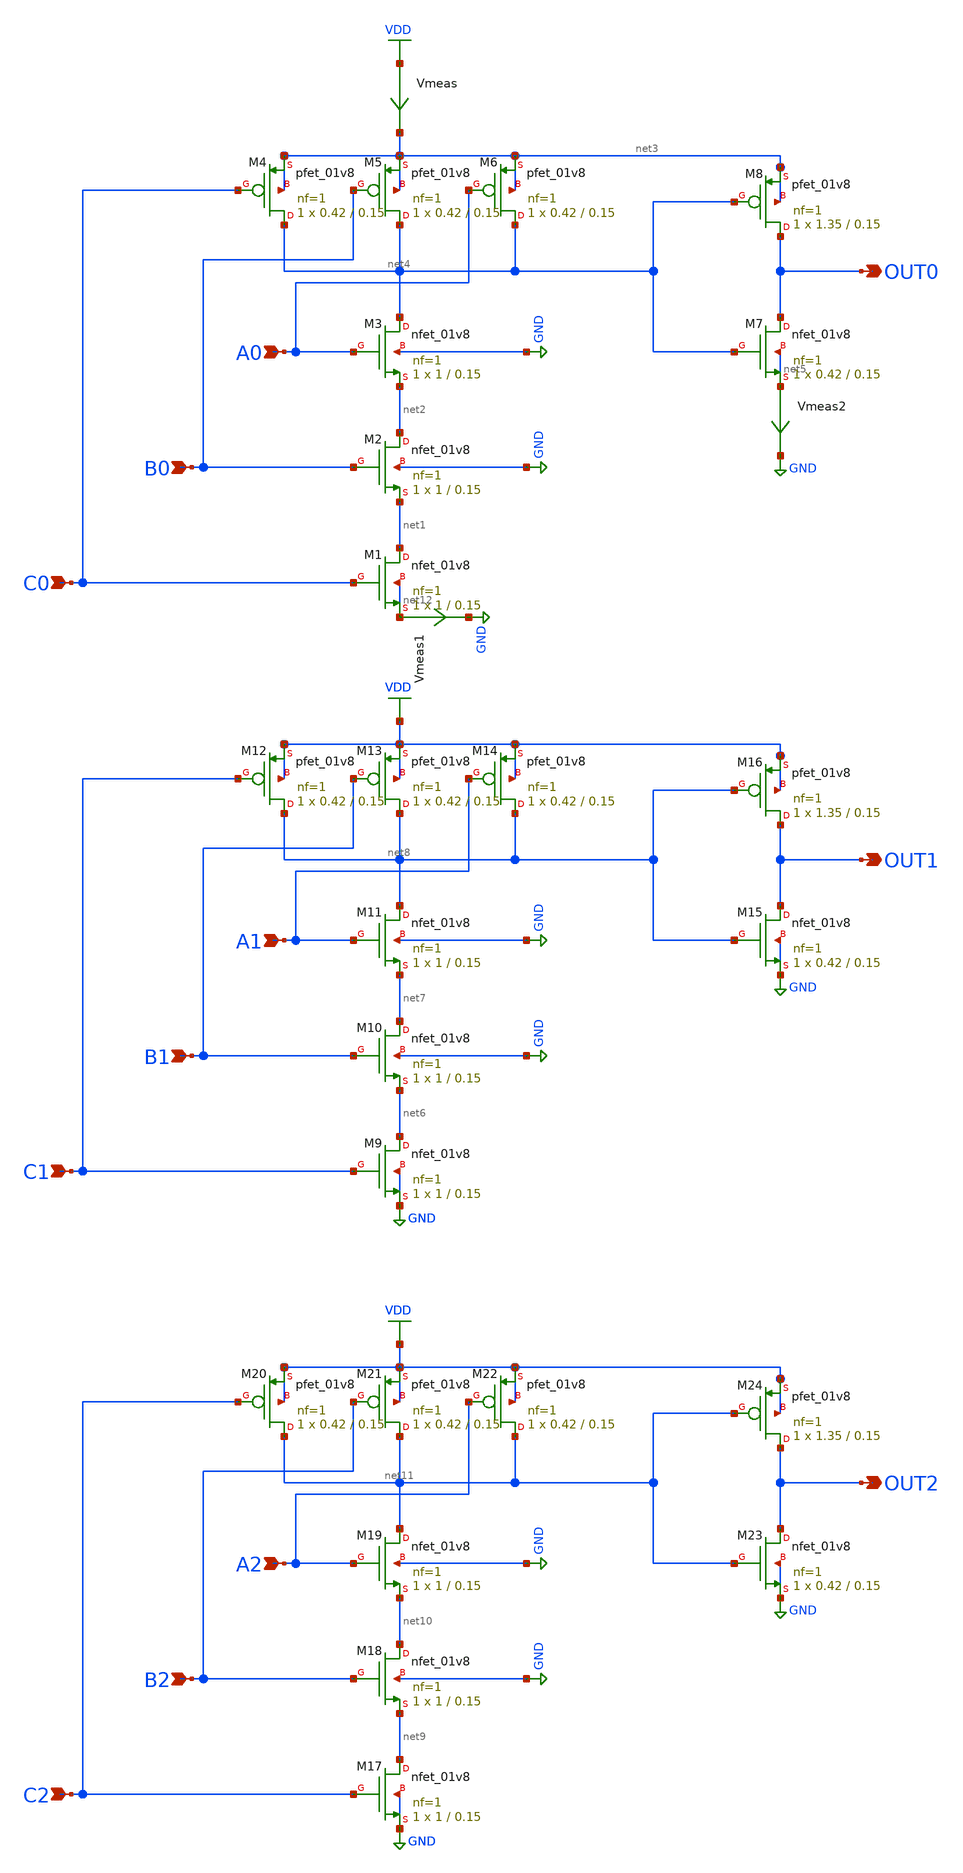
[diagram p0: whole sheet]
** sch_path: xschem/dec_cell_3.sch
**.subckt dec_cell_3 OUT0 OUT1 OUT2 C2 B2 A2 C1 B1 A1 C0 B0 A0
*.opin OUT0
*.opin OUT1
*.opin OUT2
*.ipin C2
*.ipin B2
*.ipin A2
*.ipin C1
*.ipin B1
*.ipin A1
*.ipin C0
*.ipin B0
*.ipin A0
XM1 net1 C0 net12 net12 sky130_fd_pr__nfet_01v8 L=0.15 W=1 nf=1 ad='int((nf+1)/2) * W/nf * 0.29' as='int((nf+2)/2) * W/nf * 0.29'
+ pd='2*int((nf+1)/2) * (W/nf + 0.29)' ps='2*int((nf+2)/2) * (W/nf + 0.29)' nrd='0.29 / W' nrs='0.29 / W'
+ sa=0 sb=0 sd=0 mult=1 m=1
XM2 net2 B0 net1 GND sky130_fd_pr__nfet_01v8 L=0.15 W=1 nf=1 ad='int((nf+1)/2) * W/nf * 0.29' as='int((nf+2)/2) * W/nf * 0.29'
+ pd='2*int((nf+1)/2) * (W/nf + 0.29)' ps='2*int((nf+2)/2) * (W/nf + 0.29)' nrd='0.29 / W' nrs='0.29 / W'
+ sa=0 sb=0 sd=0 mult=1 m=1
XM3 net4 A0 net2 GND sky130_fd_pr__nfet_01v8 L=0.15 W=1 nf=1 ad='int((nf+1)/2) * W/nf * 0.29' as='int((nf+2)/2) * W/nf * 0.29'
+ pd='2*int((nf+1)/2) * (W/nf + 0.29)' ps='2*int((nf+2)/2) * (W/nf + 0.29)' nrd='0.29 / W' nrs='0.29 / W'
+ sa=0 sb=0 sd=0 mult=1 m=1
XM4 net4 C0 net3 net3 sky130_fd_pr__pfet_01v8 L=0.15 W=0.42 nf=1 ad='int((nf+1)/2) * W/nf * 0.29' as='int((nf+2)/2) * W/nf * 0.29'
+ pd='2*int((nf+1)/2) * (W/nf + 0.29)' ps='2*int((nf+2)/2) * (W/nf + 0.29)' nrd='0.29 / W' nrs='0.29 / W'
+ sa=0 sb=0 sd=0 mult=1 m=1
XM5 net4 B0 net3 net3 sky130_fd_pr__pfet_01v8 L=0.15 W=0.42 nf=1 ad='int((nf+1)/2) * W/nf * 0.29' as='int((nf+2)/2) * W/nf * 0.29'
+ pd='2*int((nf+1)/2) * (W/nf + 0.29)' ps='2*int((nf+2)/2) * (W/nf + 0.29)' nrd='0.29 / W' nrs='0.29 / W'
+ sa=0 sb=0 sd=0 mult=1 m=1
XM6 net4 A0 net3 net3 sky130_fd_pr__pfet_01v8 L=0.15 W=0.42 nf=1 ad='int((nf+1)/2) * W/nf * 0.29' as='int((nf+2)/2) * W/nf * 0.29'
+ pd='2*int((nf+1)/2) * (W/nf + 0.29)' ps='2*int((nf+2)/2) * (W/nf + 0.29)' nrd='0.29 / W' nrs='0.29 / W'
+ sa=0 sb=0 sd=0 mult=1 m=1
XM7 OUT0 net4 net5 net5 sky130_fd_pr__nfet_01v8 L=0.15 W=0.42 nf=1 ad='int((nf+1)/2) * W/nf * 0.29' as='int((nf+2)/2) * W/nf * 0.29'
+ pd='2*int((nf+1)/2) * (W/nf + 0.29)' ps='2*int((nf+2)/2) * (W/nf + 0.29)' nrd='0.29 / W' nrs='0.29 / W'
+ sa=0 sb=0 sd=0 mult=1 m=1
XM8 OUT0 net4 net3 net3 sky130_fd_pr__pfet_01v8 L=0.15 W=1.35 nf=1 ad='int((nf+1)/2) * W/nf * 0.29' as='int((nf+2)/2) * W/nf * 0.29'
+ pd='2*int((nf+1)/2) * (W/nf + 0.29)' ps='2*int((nf+2)/2) * (W/nf + 0.29)' nrd='0.29 / W' nrs='0.29 / W'
+ sa=0 sb=0 sd=0 mult=1 m=1
XM9 net6 C1 GND GND sky130_fd_pr__nfet_01v8 L=0.15 W=1 nf=1 ad='int((nf+1)/2) * W/nf * 0.29' as='int((nf+2)/2) * W/nf * 0.29'
+ pd='2*int((nf+1)/2) * (W/nf + 0.29)' ps='2*int((nf+2)/2) * (W/nf + 0.29)' nrd='0.29 / W' nrs='0.29 / W'
+ sa=0 sb=0 sd=0 mult=1 m=1
XM10 net7 B1 net6 GND sky130_fd_pr__nfet_01v8 L=0.15 W=1 nf=1 ad='int((nf+1)/2) * W/nf * 0.29' as='int((nf+2)/2) * W/nf * 0.29'
+ pd='2*int((nf+1)/2) * (W/nf + 0.29)' ps='2*int((nf+2)/2) * (W/nf + 0.29)' nrd='0.29 / W' nrs='0.29 / W'
+ sa=0 sb=0 sd=0 mult=1 m=1
XM11 net8 A1 net7 GND sky130_fd_pr__nfet_01v8 L=0.15 W=1 nf=1 ad='int((nf+1)/2) * W/nf * 0.29' as='int((nf+2)/2) * W/nf * 0.29'
+ pd='2*int((nf+1)/2) * (W/nf + 0.29)' ps='2*int((nf+2)/2) * (W/nf + 0.29)' nrd='0.29 / W' nrs='0.29 / W'
+ sa=0 sb=0 sd=0 mult=1 m=1
XM12 net8 C1 VDD VDD sky130_fd_pr__pfet_01v8 L=0.15 W=0.42 nf=1 ad='int((nf+1)/2) * W/nf * 0.29' as='int((nf+2)/2) * W/nf * 0.29'
+ pd='2*int((nf+1)/2) * (W/nf + 0.29)' ps='2*int((nf+2)/2) * (W/nf + 0.29)' nrd='0.29 / W' nrs='0.29 / W'
+ sa=0 sb=0 sd=0 mult=1 m=1
XM13 net8 B1 VDD VDD sky130_fd_pr__pfet_01v8 L=0.15 W=0.42 nf=1 ad='int((nf+1)/2) * W/nf * 0.29' as='int((nf+2)/2) * W/nf * 0.29'
+ pd='2*int((nf+1)/2) * (W/nf + 0.29)' ps='2*int((nf+2)/2) * (W/nf + 0.29)' nrd='0.29 / W' nrs='0.29 / W'
+ sa=0 sb=0 sd=0 mult=1 m=1
XM14 net8 A1 VDD VDD sky130_fd_pr__pfet_01v8 L=0.15 W=0.42 nf=1 ad='int((nf+1)/2) * W/nf * 0.29' as='int((nf+2)/2) * W/nf * 0.29'
+ pd='2*int((nf+1)/2) * (W/nf + 0.29)' ps='2*int((nf+2)/2) * (W/nf + 0.29)' nrd='0.29 / W' nrs='0.29 / W'
+ sa=0 sb=0 sd=0 mult=1 m=1
XM15 OUT1 net8 GND GND sky130_fd_pr__nfet_01v8 L=0.15 W=0.42 nf=1 ad='int((nf+1)/2) * W/nf * 0.29' as='int((nf+2)/2) * W/nf * 0.29'
+ pd='2*int((nf+1)/2) * (W/nf + 0.29)' ps='2*int((nf+2)/2) * (W/nf + 0.29)' nrd='0.29 / W' nrs='0.29 / W'
+ sa=0 sb=0 sd=0 mult=1 m=1
XM16 OUT1 net8 VDD VDD sky130_fd_pr__pfet_01v8 L=0.15 W=1.35 nf=1 ad='int((nf+1)/2) * W/nf * 0.29' as='int((nf+2)/2) * W/nf * 0.29'
+ pd='2*int((nf+1)/2) * (W/nf + 0.29)' ps='2*int((nf+2)/2) * (W/nf + 0.29)' nrd='0.29 / W' nrs='0.29 / W'
+ sa=0 sb=0 sd=0 mult=1 m=1
XM17 net9 C2 GND GND sky130_fd_pr__nfet_01v8 L=0.15 W=1 nf=1 ad='int((nf+1)/2) * W/nf * 0.29' as='int((nf+2)/2) * W/nf * 0.29'
+ pd='2*int((nf+1)/2) * (W/nf + 0.29)' ps='2*int((nf+2)/2) * (W/nf + 0.29)' nrd='0.29 / W' nrs='0.29 / W'
+ sa=0 sb=0 sd=0 mult=1 m=1
XM18 net10 B2 net9 GND sky130_fd_pr__nfet_01v8 L=0.15 W=1 nf=1 ad='int((nf+1)/2) * W/nf * 0.29' as='int((nf+2)/2) * W/nf * 0.29'
+ pd='2*int((nf+1)/2) * (W/nf + 0.29)' ps='2*int((nf+2)/2) * (W/nf + 0.29)' nrd='0.29 / W' nrs='0.29 / W'
+ sa=0 sb=0 sd=0 mult=1 m=1
XM19 net11 A2 net10 GND sky130_fd_pr__nfet_01v8 L=0.15 W=1 nf=1 ad='int((nf+1)/2) * W/nf * 0.29' as='int((nf+2)/2) * W/nf * 0.29'
+ pd='2*int((nf+1)/2) * (W/nf + 0.29)' ps='2*int((nf+2)/2) * (W/nf + 0.29)' nrd='0.29 / W' nrs='0.29 / W'
+ sa=0 sb=0 sd=0 mult=1 m=1
XM20 net11 C2 VDD VDD sky130_fd_pr__pfet_01v8 L=0.15 W=0.42 nf=1 ad='int((nf+1)/2) * W/nf * 0.29' as='int((nf+2)/2) * W/nf * 0.29'
+ pd='2*int((nf+1)/2) * (W/nf + 0.29)' ps='2*int((nf+2)/2) * (W/nf + 0.29)' nrd='0.29 / W' nrs='0.29 / W'
+ sa=0 sb=0 sd=0 mult=1 m=1
XM21 net11 B2 VDD VDD sky130_fd_pr__pfet_01v8 L=0.15 W=0.42 nf=1 ad='int((nf+1)/2) * W/nf * 0.29' as='int((nf+2)/2) * W/nf * 0.29'
+ pd='2*int((nf+1)/2) * (W/nf + 0.29)' ps='2*int((nf+2)/2) * (W/nf + 0.29)' nrd='0.29 / W' nrs='0.29 / W'
+ sa=0 sb=0 sd=0 mult=1 m=1
XM22 net11 A2 VDD VDD sky130_fd_pr__pfet_01v8 L=0.15 W=0.42 nf=1 ad='int((nf+1)/2) * W/nf * 0.29' as='int((nf+2)/2) * W/nf * 0.29'
+ pd='2*int((nf+1)/2) * (W/nf + 0.29)' ps='2*int((nf+2)/2) * (W/nf + 0.29)' nrd='0.29 / W' nrs='0.29 / W'
+ sa=0 sb=0 sd=0 mult=1 m=1
XM23 OUT2 net11 GND GND sky130_fd_pr__nfet_01v8 L=0.15 W=0.42 nf=1 ad='int((nf+1)/2) * W/nf * 0.29' as='int((nf+2)/2) * W/nf * 0.29'
+ pd='2*int((nf+1)/2) * (W/nf + 0.29)' ps='2*int((nf+2)/2) * (W/nf + 0.29)' nrd='0.29 / W' nrs='0.29 / W'
+ sa=0 sb=0 sd=0 mult=1 m=1
XM24 OUT2 net11 VDD VDD sky130_fd_pr__pfet_01v8 L=0.15 W=1.35 nf=1 ad='int((nf+1)/2) * W/nf * 0.29' as='int((nf+2)/2) * W/nf * 0.29'
+ pd='2*int((nf+1)/2) * (W/nf + 0.29)' ps='2*int((nf+2)/2) * (W/nf + 0.29)' nrd='0.29 / W' nrs='0.29 / W'
+ sa=0 sb=0 sd=0 mult=1 m=1
Vmeas VDD net3 0
.save i(vmeas)
Vmeas1 net12 GND 0
.save i(vmeas1)
Vmeas2 net5 GND 0
.save i(vmeas2)
**.ends
.GLOBAL VDD
.GLOBAL GND
.end
